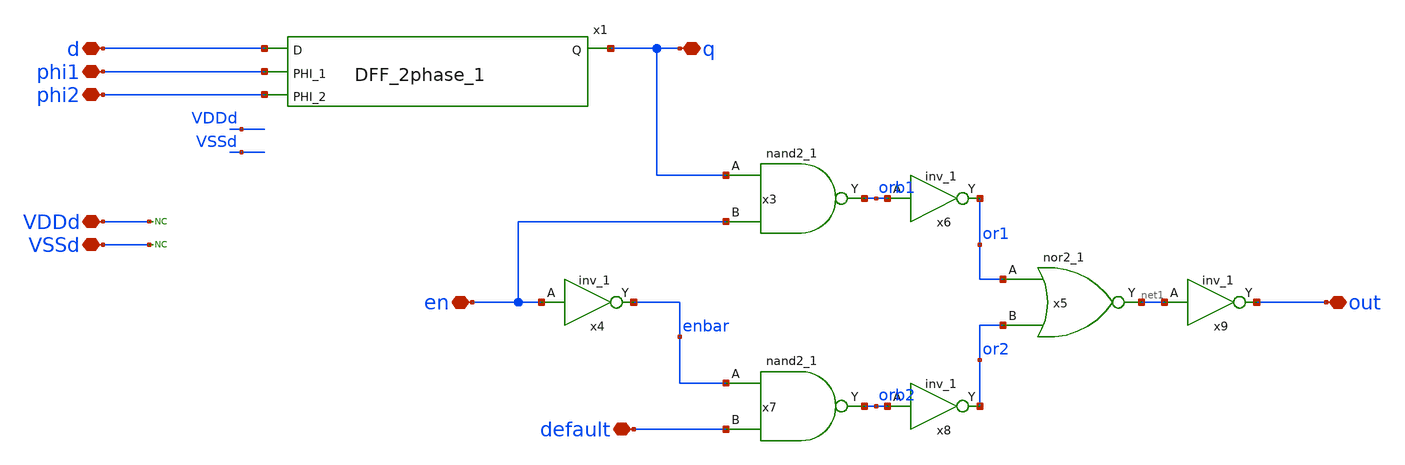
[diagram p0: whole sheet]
** sch_path: designs/libs/qw_core_analog/Register_unitcell/Register_unitcell.sch
**.subckt Register_unitcell phi1 phi2 d q en default out VDDd VSSd
*.iopin phi1
*.iopin phi2
*.iopin d
*.iopin q
*.iopin en
*.iopin default
*.iopin out
*.iopin VDDd
*.iopin VSSd
x1 d q phi1 phi2 DFF_2phase_1
x3 q en VSSd VDDd VSSd VDDd orb1 gf180mcu_fd_sc_mcu9t5v0__nand2_1
x4 en VSSd VDDd VSSd VDDd enbar gf180mcu_fd_sc_mcu9t5v0__inv_1
x5 or1 or2 VSSd VDDd VSSd VDDd net1 gf180mcu_fd_sc_mcu9t5v0__nor2_1
x6 orb1 VSSd VDDd VSSd VDDd or1 gf180mcu_fd_sc_mcu9t5v0__inv_1
x7 enbar default VSSd VDDd VSSd VDDd orb2 gf180mcu_fd_sc_mcu9t5v0__nand2_1
x8 orb2 VSSd VDDd VSSd VDDd or2 gf180mcu_fd_sc_mcu9t5v0__inv_1
x9 net1 VSSd VDDd VSSd VDDd out gf180mcu_fd_sc_mcu9t5v0__inv_1
* noconn VDDd
* noconn VSSd
**.ends

* expanding   symbol:  switch_matrix_gf180mcu_9t5v0-main/DFF_2phase_1/DFF_2phase_1.sym # of pins=4
** sym_path: designs/switch_matrix_gf180mcu_9t5v0-main/designs/libs/core_swmatrix/DFF_2phase_1.sym
** sch_path: designs/switch_matrix_gf180mcu_9t5v0-main/designs/libs/core_swmatrix/DFF_2phase_1.sch
.subckt DFF_2phase_1 D Q PHI_1 PHI_2
*.ipin D
*.ipin PHI_1
*.ipin PHI_2
*.opin Q
xmain D PHI_1 out_m VDDd VDDd VSSd VSSd gf180mcu_fd_sc_mcu9t5v0__latq_1
xsecondary out_m PHI_2 Q VDDd VDDd VSSd VSSd gf180mcu_fd_sc_mcu9t5v0__latq_1
.ends

.end
